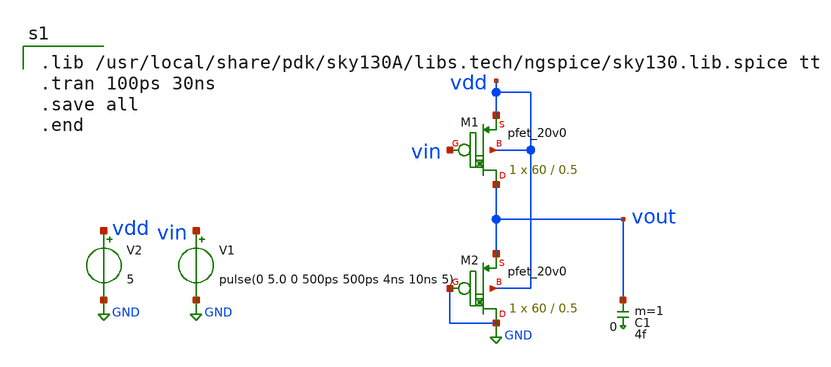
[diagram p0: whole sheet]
** sch_path: xschem/PMOS_inv.sch
**.subckt PMOS_inv
V1 vin GND pulse(0 5.0 0 500ps 500ps 4ns 10ns 5)
V2 vdd GND 5
C1 vout 0 4f m=1
XM1 vout vin vdd vdd sky130_fd_pr__pfet_20v0 L=0.5 W=60 m=1
XM2 GND GND vout vdd sky130_fd_pr__pfet_20v0 L=0.5 W=60 m=1
**** begin user architecture code

.lib /usr/local/share/pdk/sky130A/libs.tech/ngspice/sky130.lib.spice tt
.tran 100ps 30ns
.save all
.end

**** end user architecture code
**.ends
.GLOBAL GND
.end
